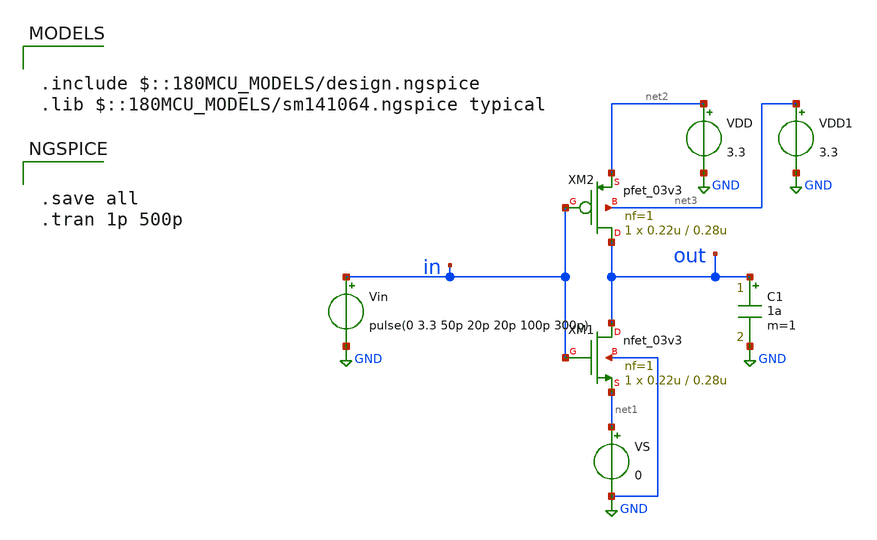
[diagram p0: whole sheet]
** sch_path: gf_tutorials/test_inverter.sch
**.subckt test_inverter
XM1 out in net1 GND nfet_03v3 L=0.28u W=0.22u nf=1 ad='int((nf+1)/2) * W/nf * 0.18u' as='int((nf+2)/2) * W/nf * 0.18u'
+ pd='2*int((nf+1)/2) * (W/nf + 0.18u)' ps='2*int((nf+2)/2) * (W/nf + 0.18u)' nrd='0.18u / W' nrs='0.18u / W'
+ sa=0 sb=0 sd=0 m=1
XM2 out in net2 net3 pfet_03v3 L=0.28u W=0.22u nf=1 ad='int((nf+1)/2) * W/nf * 0.18u' as='int((nf+2)/2) * W/nf * 0.18u'
+ pd='2*int((nf+1)/2) * (W/nf + 0.18u)' ps='2*int((nf+2)/2) * (W/nf + 0.18u)' nrd='0.18u / W' nrs='0.18u / W'
+ sa=0 sb=0 sd=0 m=1
Vin in GND pulse(0 3.3 50p 20p 20p 100p 300p)
VDD net2 GND 3.3
VS net1 GND 0
C1 out GND 1a m=1
VDD1 net3 GND 3.3
**** begin user architecture code

.include $::180MCU_MODELS/design.ngspice
.lib $::180MCU_MODELS/sm141064.ngspice typical



.save all
.tran 1p 500p


**** end user architecture code
**.ends
.GLOBAL GND
.end
